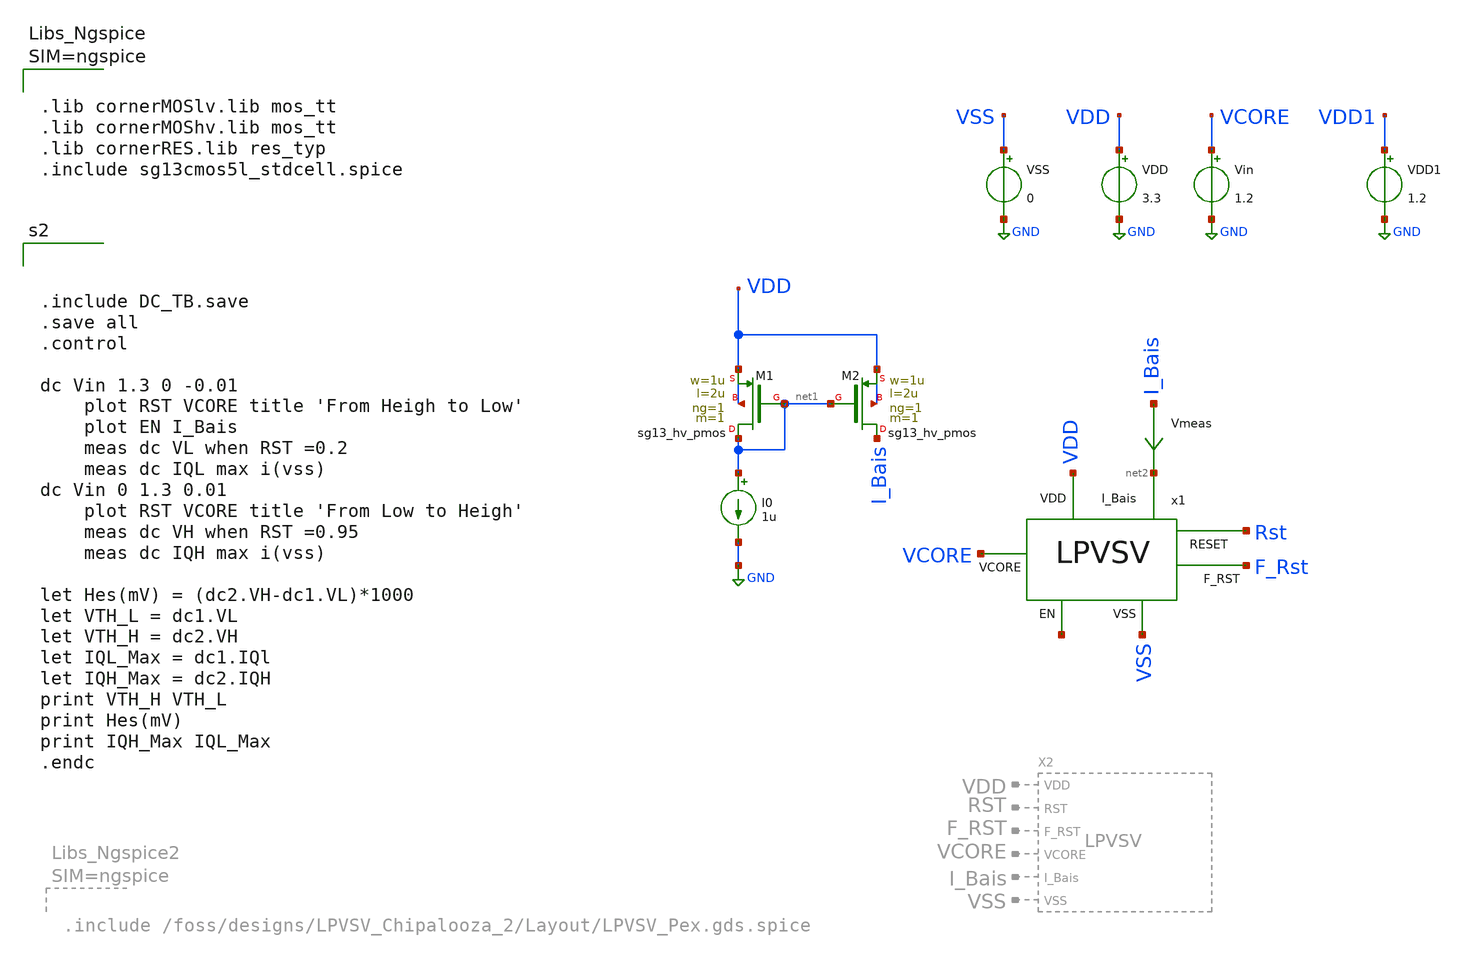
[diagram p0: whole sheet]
** sch_path: Simulation/DC_TB.sch
**.subckt DC_TB
VDD VDD GND 3.3
VSS VSS GND 0
Vin VCORE GND 1.2
I0 net1 GND 1u
x1 VDD VCORE net2 Rst F_Rst VSS net3 LPVSV
XM1 net1 net1 VDD VDD sg13_hv_pmos w=1u l=2u ng=1 m=1 mm_ok=1
XM2 I_Bais net1 VDD VDD sg13_hv_pmos w=1u l=2u ng=1 m=1 mm_ok=1
Vmeas I_Bais net2 0
.save i(vmeas)
VDD1 VDD1 GND 1.2
**** begin user architecture code



.include DC_TB.save
.save all
.control

dc Vin 1.3 0 -0.01
	plot RST VCORE title 'From Heigh to Low'
	plot EN I_Bais
	meas dc VL when RST =0.2
	meas dc IQL max i(vss)
dc Vin 0 1.3 0.01
	plot RST VCORE title 'From Low to Heigh'
	meas dc VH when RST =0.95
	meas dc IQH max i(vss)

let Hes(mV) = (dc2.VH-dc1.VL)*1000
let VTH_L = dc1.VL
let VTH_H = dc2.VH
let IQL_Max = dc1.IQl
let IQH_Max = dc2.IQH
print VTH_H VTH_L
print Hes(mV)
print IQH_Max IQL_Max
.endc




.options rshunt = 1e15
.options gmin=1e-9
.options reltol = 0.01 abstol = 1p
.option filetype=ascii





.lib cornerMOSlv.lib mos_tt
.lib cornerMOShv.lib mos_tt
.lib cornerRES.lib res_typ
.include sg13cmos5l_stdcell.spice



**** end user architecture code
**.ends
.GLOBAL GND
.end
